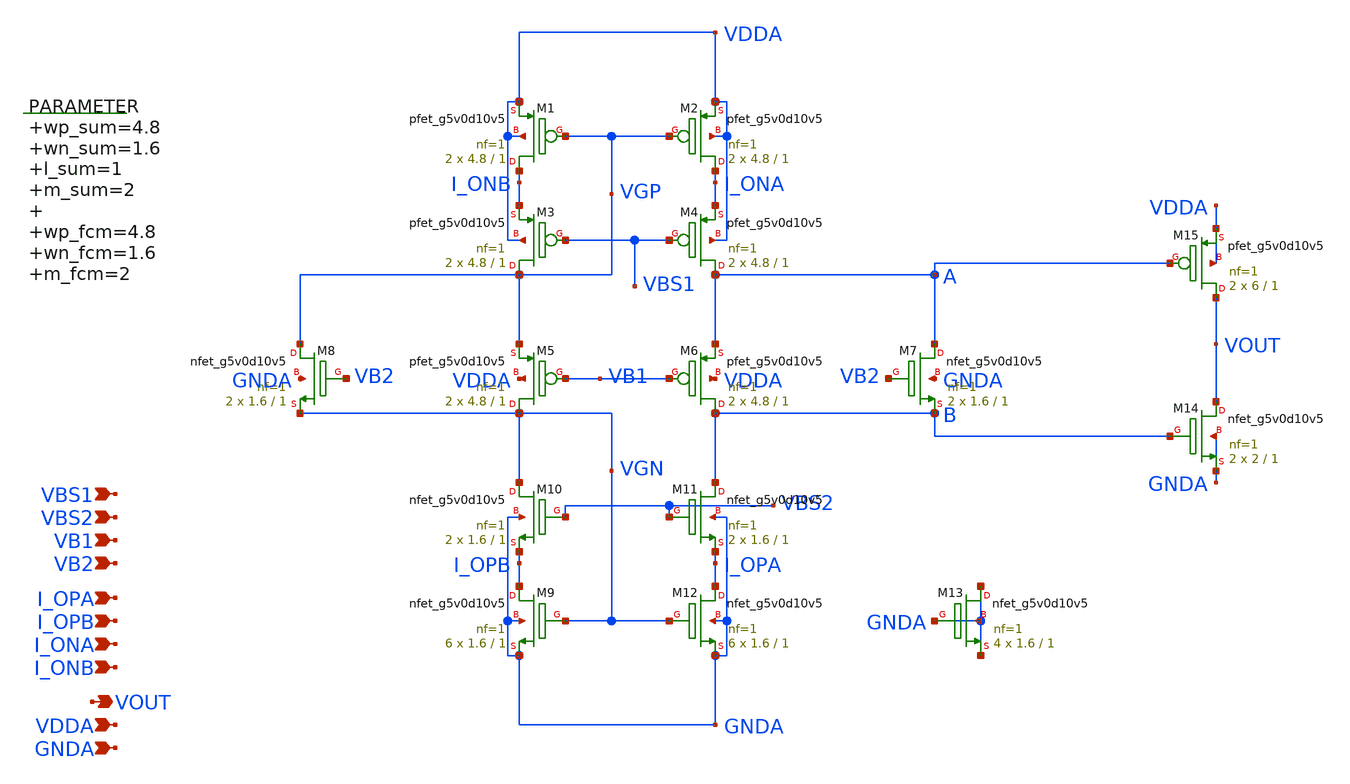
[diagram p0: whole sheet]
** sch_path: xschem/folded_cascode.sch
**.subckt folded_cascode I_OPA I_OPB I_ONA I_ONB VOUT VBS1 VBS2 VB1 VB2 VDDA GNDA
*.ipin I_OPA
*.ipin I_OPB
*.ipin I_ONA
*.ipin I_ONB
*.opin VOUT
*.ipin VBS1
*.ipin VBS2
*.ipin VB1
*.ipin VB2
*.ipin VDDA
*.ipin GNDA
.param wp_sum=4.8 wn_sum=1.6 l_sum=1 m_sum=2 wp_fcm=4.8 wn_fcm=1.6 m_fcm=2

XM1 I_ONB VGP VDDA VDDA sky130_fd_pr__pfet_g5v0d10v5 L=1 W=4.8 nf=1 ad='int((nf+1)/2) * W/nf * 0.29'
+ as='int((nf+2)/2) * W/nf * 0.29' pd='2*int((nf+1)/2) * (W/nf + 0.29)' ps='2*int((nf+2)/2) * (W/nf + 0.29)'
+ nrd='0.29 / W' nrs='0.29 / W' sa=0 sb=0 sd=0 mult=2 m=2
XM8 VGP VB2 VGN GNDA sky130_fd_pr__nfet_g5v0d10v5 L=1 W=1.6 nf=1 ad='int((nf+1)/2) * W/nf * 0.29' as='int((nf+2)/2) * W/nf * 0.29'
+ pd='2*int((nf+1)/2) * (W/nf + 0.29)' ps='2*int((nf+2)/2) * (W/nf + 0.29)' nrd='0.29 / W' nrs='0.29 / W'
+ sa=0 sb=0 sd=0 mult=2 m=2
XM13 GNDA GNDA GNDA GNDA sky130_fd_pr__nfet_g5v0d10v5 L=1 W=1.6 nf=1 ad='int((nf+1)/2) * W/nf * 0.29'
+ as='int((nf+2)/2) * W/nf * 0.29' pd='2*int((nf+1)/2) * (W/nf + 0.29)' ps='2*int((nf+2)/2) * (W/nf + 0.29)'
+ nrd='0.29 / W' nrs='0.29 / W' sa=0 sb=0 sd=0 mult=4 m=4
XM2 I_ONA VGP VDDA VDDA sky130_fd_pr__pfet_g5v0d10v5 L=1 W=4.8 nf=1 ad='int((nf+1)/2) * W/nf * 0.29'
+ as='int((nf+2)/2) * W/nf * 0.29' pd='2*int((nf+1)/2) * (W/nf + 0.29)' ps='2*int((nf+2)/2) * (W/nf + 0.29)'
+ nrd='0.29 / W' nrs='0.29 / W' sa=0 sb=0 sd=0 mult=2 m=2
XM3 VGP VBS1 I_ONB VDDA sky130_fd_pr__pfet_g5v0d10v5 L=1 W=4.8 nf=1 ad='int((nf+1)/2) * W/nf * 0.29'
+ as='int((nf+2)/2) * W/nf * 0.29' pd='2*int((nf+1)/2) * (W/nf + 0.29)' ps='2*int((nf+2)/2) * (W/nf + 0.29)'
+ nrd='0.29 / W' nrs='0.29 / W' sa=0 sb=0 sd=0 mult=2 m=2
XM4 A VBS1 I_ONA VDDA sky130_fd_pr__pfet_g5v0d10v5 L=1 W=4.8 nf=1 ad='int((nf+1)/2) * W/nf * 0.29' as='int((nf+2)/2) * W/nf * 0.29'
+ pd='2*int((nf+1)/2) * (W/nf + 0.29)' ps='2*int((nf+2)/2) * (W/nf + 0.29)' nrd='0.29 / W' nrs='0.29 / W'
+ sa=0 sb=0 sd=0 mult=2 m=2
XM5 VGN VB1 VGP VDDA sky130_fd_pr__pfet_g5v0d10v5 L=1 W=4.8 nf=1 ad='int((nf+1)/2) * W/nf * 0.29' as='int((nf+2)/2) * W/nf * 0.29'
+ pd='2*int((nf+1)/2) * (W/nf + 0.29)' ps='2*int((nf+2)/2) * (W/nf + 0.29)' nrd='0.29 / W' nrs='0.29 / W'
+ sa=0 sb=0 sd=0 mult=2 m=2
XM6 B VB1 A VDDA sky130_fd_pr__pfet_g5v0d10v5 L=1 W=4.8 nf=1 ad='int((nf+1)/2) * W/nf * 0.29' as='int((nf+2)/2) * W/nf * 0.29'
+ pd='2*int((nf+1)/2) * (W/nf + 0.29)' ps='2*int((nf+2)/2) * (W/nf + 0.29)' nrd='0.29 / W' nrs='0.29 / W'
+ sa=0 sb=0 sd=0 mult=2 m=2
XM7 A VB2 B GNDA sky130_fd_pr__nfet_g5v0d10v5 L=1 W=1.6 nf=1 ad='int((nf+1)/2) * W/nf * 0.29' as='int((nf+2)/2) * W/nf * 0.29'
+ pd='2*int((nf+1)/2) * (W/nf + 0.29)' ps='2*int((nf+2)/2) * (W/nf + 0.29)' nrd='0.29 / W' nrs='0.29 / W'
+ sa=0 sb=0 sd=0 mult=2 m=2
XM10 VGN VBS2 I_OPB GNDA sky130_fd_pr__nfet_g5v0d10v5 L=1 W=1.6 nf=1 ad='int((nf+1)/2) * W/nf * 0.29'
+ as='int((nf+2)/2) * W/nf * 0.29' pd='2*int((nf+1)/2) * (W/nf + 0.29)' ps='2*int((nf+2)/2) * (W/nf + 0.29)'
+ nrd='0.29 / W' nrs='0.29 / W' sa=0 sb=0 sd=0 mult=2 m=2
XM11 B VBS2 I_OPA GNDA sky130_fd_pr__nfet_g5v0d10v5 L=1 W=1.6 nf=1 ad='int((nf+1)/2) * W/nf * 0.29' as='int((nf+2)/2) * W/nf * 0.29'
+ pd='2*int((nf+1)/2) * (W/nf + 0.29)' ps='2*int((nf+2)/2) * (W/nf + 0.29)' nrd='0.29 / W' nrs='0.29 / W'
+ sa=0 sb=0 sd=0 mult=2 m=2
XM9 I_OPB VGN GNDA GNDA sky130_fd_pr__nfet_g5v0d10v5 L=1 W=1.6 nf=1 ad='int((nf+1)/2) * W/nf * 0.29'
+ as='int((nf+2)/2) * W/nf * 0.29' pd='2*int((nf+1)/2) * (W/nf + 0.29)' ps='2*int((nf+2)/2) * (W/nf + 0.29)'
+ nrd='0.29 / W' nrs='0.29 / W' sa=0 sb=0 sd=0 mult=6 m=6
XM12 I_OPA VGN GNDA GNDA sky130_fd_pr__nfet_g5v0d10v5 L=1 W=1.6 nf=1 ad='int((nf+1)/2) * W/nf * 0.29'
+ as='int((nf+2)/2) * W/nf * 0.29' pd='2*int((nf+1)/2) * (W/nf + 0.29)' ps='2*int((nf+2)/2) * (W/nf + 0.29)'
+ nrd='0.29 / W' nrs='0.29 / W' sa=0 sb=0 sd=0 mult=6 m=6
XM14 VOUT B GNDA GNDA sky130_fd_pr__nfet_g5v0d10v5 L=1 W=2 nf=1 ad='int((nf+1)/2) * W/nf * 0.29' as='int((nf+2)/2) * W/nf * 0.29'
+ pd='2*int((nf+1)/2) * (W/nf + 0.29)' ps='2*int((nf+2)/2) * (W/nf + 0.29)' nrd='0.29 / W' nrs='0.29 / W'
+ sa=0 sb=0 sd=0 mult=2 m=2
XM15 VOUT A VDDA VDDA sky130_fd_pr__pfet_g5v0d10v5 L=1 W=6 nf=1 ad='int((nf+1)/2) * W/nf * 0.29' as='int((nf+2)/2) * W/nf * 0.29'
+ pd='2*int((nf+1)/2) * (W/nf + 0.29)' ps='2*int((nf+2)/2) * (W/nf + 0.29)' nrd='0.29 / W' nrs='0.29 / W'
+ sa=0 sb=0 sd=0 mult=2 m=2
**.ends
.end
